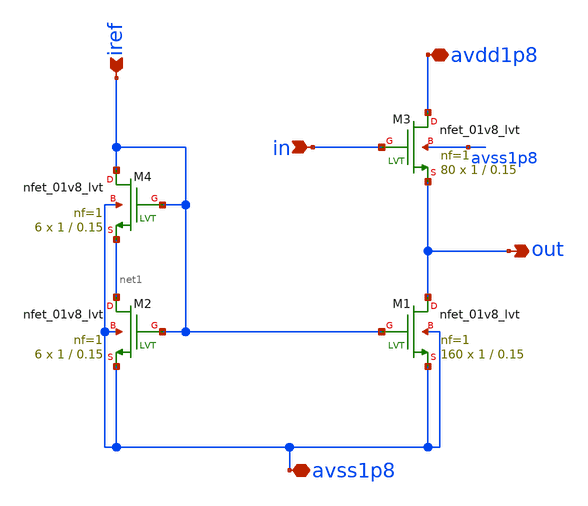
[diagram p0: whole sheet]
** sch_path: xschem/source_follower_buff_nmos.sch
**.subckt source_follower_buff_nmos avdd1p8 avss1p8 out in iref
*.iopin avdd1p8
*.iopin avss1p8
*.opin out
*.ipin in
*.ipin iref
XM2 net1 iref avss1p8 avss1p8 sky130_fd_pr__nfet_01v8_lvt L=0.15 W=1 nf=1 ad='int((nf+1)/2) * W/nf * 0.29'
+ as='int((nf+2)/2) * W/nf * 0.29' pd='2*int((nf+1)/2) * (W/nf + 0.29)' ps='2*int((nf+2)/2) * (W/nf + 0.29)'
+ nrd='0.29 / W' nrs='0.29 / W' sa=0 sb=0 sd=0 mult=6 m=6
XM1 out iref avss1p8 avss1p8 sky130_fd_pr__nfet_01v8_lvt L=0.15 W=1 nf=1 ad='int((nf+1)/2) * W/nf * 0.29'
+ as='int((nf+2)/2) * W/nf * 0.29' pd='2*int((nf+1)/2) * (W/nf + 0.29)' ps='2*int((nf+2)/2) * (W/nf + 0.29)'
+ nrd='0.29 / W' nrs='0.29 / W' sa=0 sb=0 sd=0 mult=160 m=160
XM3 avdd1p8 in out avss1p8 sky130_fd_pr__nfet_01v8_lvt L=0.15 W=1 nf=1 ad='int((nf+1)/2) * W/nf * 0.29'
+ as='int((nf+2)/2) * W/nf * 0.29' pd='2*int((nf+1)/2) * (W/nf + 0.29)' ps='2*int((nf+2)/2) * (W/nf + 0.29)'
+ nrd='0.29 / W' nrs='0.29 / W' sa=0 sb=0 sd=0 mult=80 m=80
XM4 iref iref net1 avss1p8 sky130_fd_pr__nfet_01v8_lvt L=0.15 W=1 nf=1 ad='int((nf+1)/2) * W/nf * 0.29'
+ as='int((nf+2)/2) * W/nf * 0.29' pd='2*int((nf+1)/2) * (W/nf + 0.29)' ps='2*int((nf+2)/2) * (W/nf + 0.29)'
+ nrd='0.29 / W' nrs='0.29 / W' sa=0 sb=0 sd=0 mult=6 m=6
**.ends
.end
